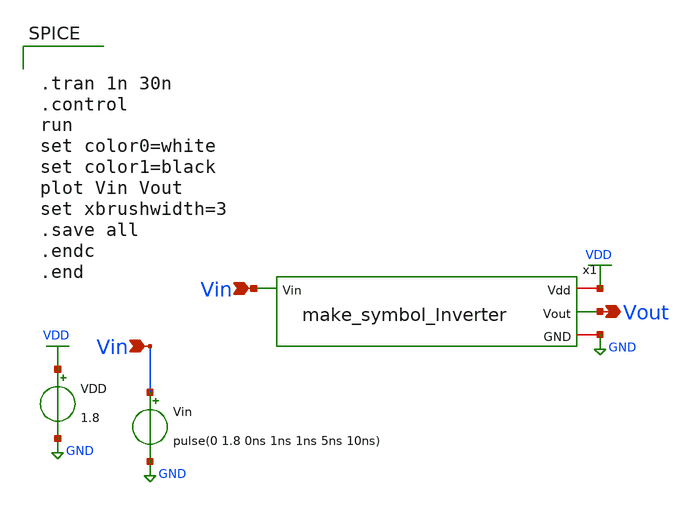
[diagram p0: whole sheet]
** sch_path: xschem/Transient_Analysis_Inverter_sym_test_banch.sch
**.subckt Transient_Analysis_Inverter_sym_test_banch Vin Vin Vout
*.ipin Vin
*.ipin Vin
*.opin Vout
VDD VDD GND 1.8
Vin Vin GND pulse(0 1.8 0ns 1ns 1ns 5ns 10ns)
x1 VDD Vin Vout GND make_symbol_Inverter
**** begin user architecture code


.lib /usr/local/share/pdk/sky130A/libs.tech/ngspice/sky130.lib.spice tt

.save all





.tran 1n 30n
.control
run
set color0=white
set color1=black
plot Vin Vout
set xbrushwidth=3
.save all
.endc
.end


**** end user architecture code
**.ends

* expanding   symbol:  make_symbol_Inverter.sym # of pins=4
** sym_path: xschem/make_symbol_Inverter.sym
** sch_path: xschem/make_symbol_Inverter.sch
.subckt make_symbol_Inverter Vdd Vin Vout GND
*.ipin Vin
*.opin Vout
*.iopin Vdd
*.iopin GND
XM1 Vout Vin Vdd Vdd sky130_fd_pr__pfet_01v8 L=0.15 W=1 nf=1 ad='int((nf+1)/2) * W/nf * 0.29' as='int((nf+2)/2) * W/nf * 0.29'
+ pd='2*int((nf+1)/2) * (W/nf + 0.29)' ps='2*int((nf+2)/2) * (W/nf + 0.29)' nrd='0.29 / W' nrs='0.29 / W'
+ sa=0 sb=0 sd=0 mult=1 m=1
XM2 Vout Vin GND GND sky130_fd_pr__nfet_01v8 L=0.15 W=1 nf=1 ad='int((nf+1)/2) * W/nf * 0.29' as='int((nf+2)/2) * W/nf * 0.29'
+ pd='2*int((nf+1)/2) * (W/nf + 0.29)' ps='2*int((nf+2)/2) * (W/nf + 0.29)' nrd='0.29 / W' nrs='0.29 / W'
+ sa=0 sb=0 sd=0 mult=1 m=1
.ends

.GLOBAL VDD
.GLOBAL GND
.end
